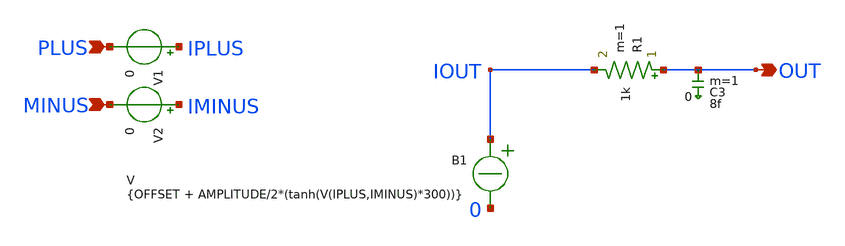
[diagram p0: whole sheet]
** sch_path: xschem_library/ngspice/comp_ngspice.sch
**.subckt comp_ngspice PLUS MINUS OUT
*.ipin PLUS
*.ipin MINUS
*.opin OUT
B1 IOUT 0 V = {OFFSET + AMPLITUDE/2*(tanh(V(IPLUS,IMINUS)*300))}
R1 OUT IOUT 1k m=1
C3 OUT 0 8f m=1
V1 IPLUS PLUS 0
V2 IMINUS MINUS 0
**.ends
.end
